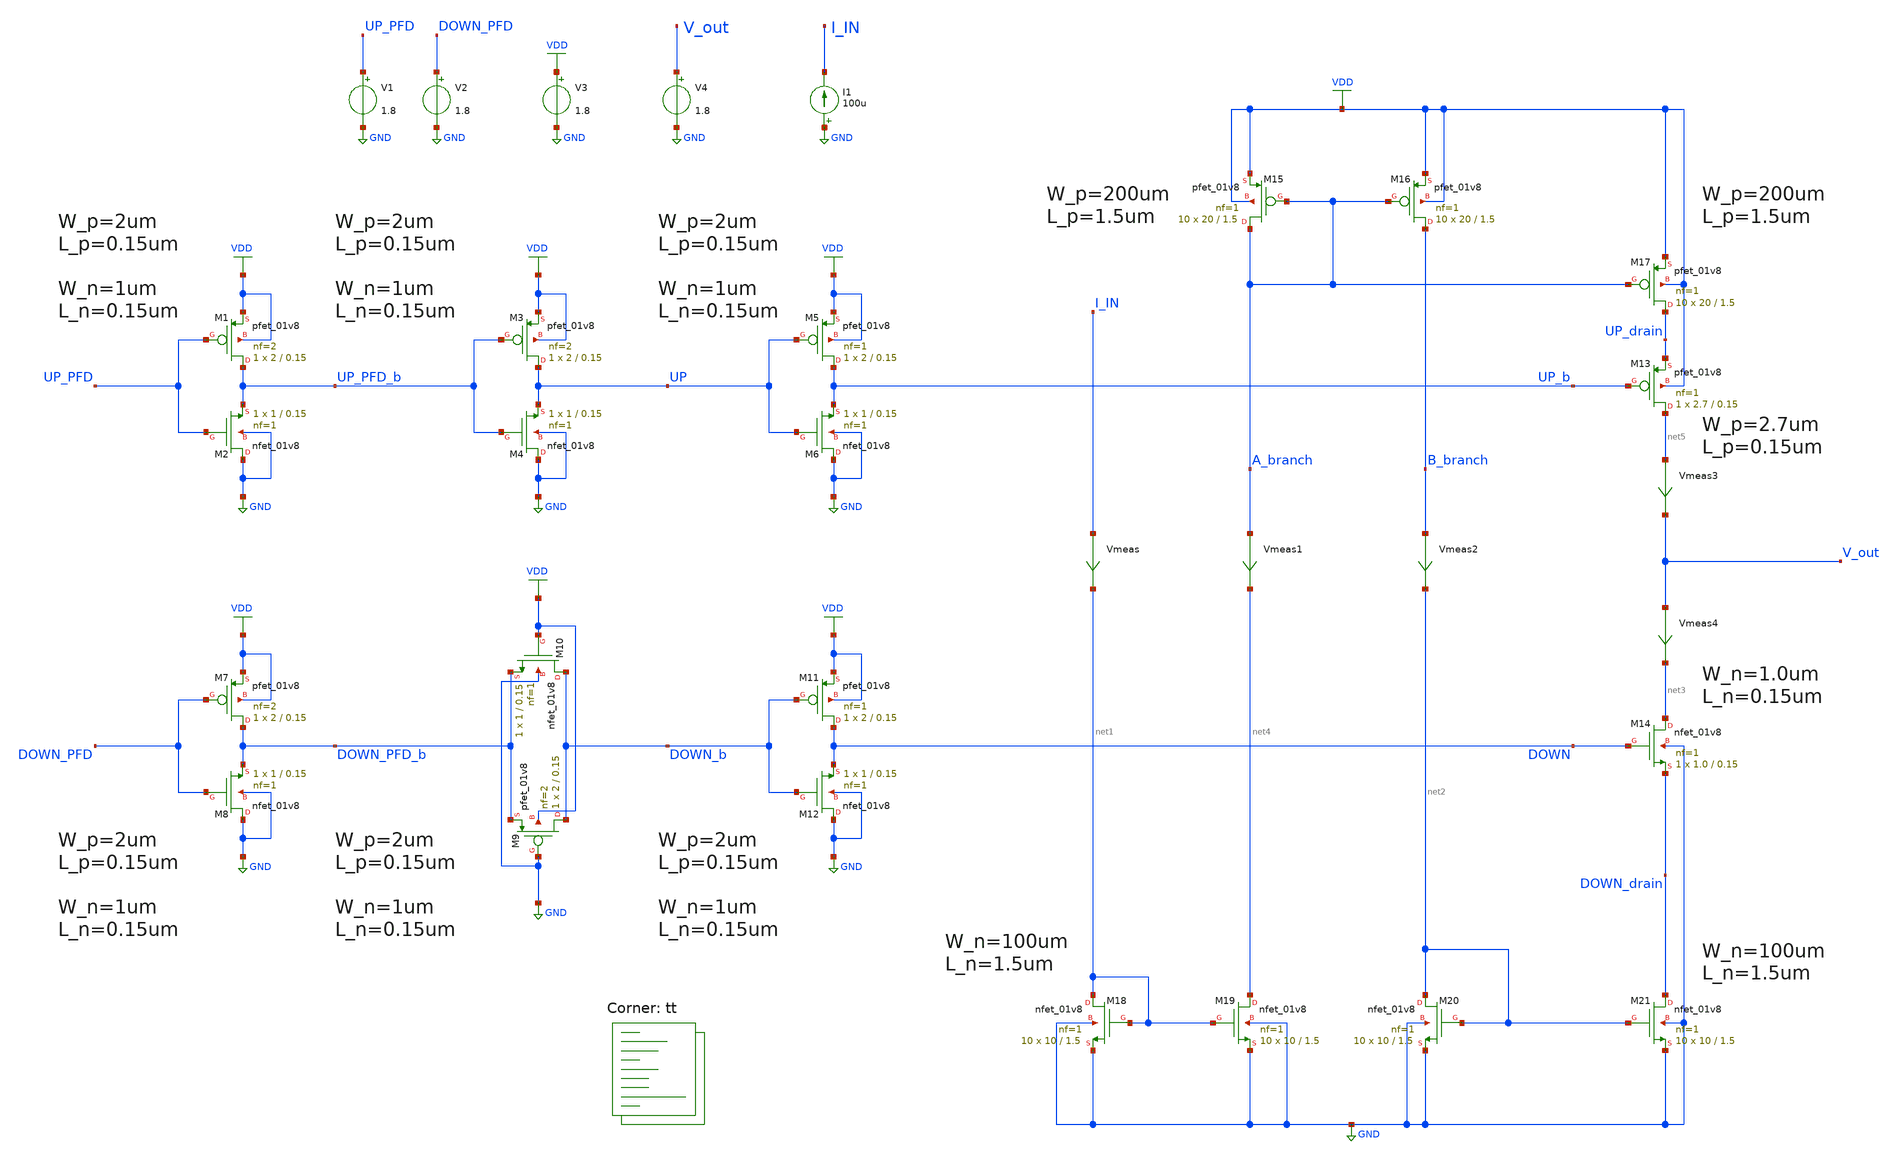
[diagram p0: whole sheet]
** sch_path: projects/pll/charge_pump/xschem_ngspice/charge_pump_DC3.sch
**.subckt charge_pump_DC3
XM18 net1 net1 GND GND sky130_fd_pr__nfet_01v8 L=1.5 W=10 nf=1 ad='int((nf+1)/2) * W/nf * 0.29' as='int((nf+2)/2) * W/nf * 0.29'
+ pd='2*int((nf+1)/2) * (W/nf + 0.29)' ps='2*int((nf+2)/2) * (W/nf + 0.29)' nrd='0.29 / W' nrs='0.29 / W'
+ sa=0 sb=0 sd=0 mult=10 m=10
XM19 net4 net1 GND GND sky130_fd_pr__nfet_01v8 L=1.5 W=10 nf=1 ad='int((nf+1)/2) * W/nf * 0.29' as='int((nf+2)/2) * W/nf * 0.29'
+ pd='2*int((nf+1)/2) * (W/nf + 0.29)' ps='2*int((nf+2)/2) * (W/nf + 0.29)' nrd='0.29 / W' nrs='0.29 / W'
+ sa=0 sb=0 sd=0 mult=10 m=10
Vmeas I_IN net1 0
.save i(vmeas)
XM13 net5 UP_b UP_drain VDD sky130_fd_pr__pfet_01v8 L=0.15 W=2.7 nf=1 ad='int((nf+1)/2) * W/nf * 0.29'
+ as='int((nf+2)/2) * W/nf * 0.29' pd='2*int((nf+1)/2) * (W/nf + 0.29)' ps='2*int((nf+2)/2) * (W/nf + 0.29)'
+ nrd='0.29 / W' nrs='0.29 / W' sa=0 sb=0 sd=0 mult=1 m=1
Vmeas3 net5 V_out 0
.save i(vmeas3)
Vmeas4 V_out net3 0
.save i(vmeas4)
XM14 net3 DOWN DOWN_drain GND sky130_fd_pr__nfet_01v8 L=0.15 W=1.0 nf=1 ad='int((nf+1)/2) * W/nf * 0.29'
+ as='int((nf+2)/2) * W/nf * 0.29' pd='2*int((nf+1)/2) * (W/nf + 0.29)' ps='2*int((nf+2)/2) * (W/nf + 0.29)'
+ nrd='0.29 / W' nrs='0.29 / W' sa=0 sb=0 sd=0 mult=1 m=1
XM17 UP_drain A_branch VDD VDD sky130_fd_pr__pfet_01v8 L=1.5 W=20 nf=1 ad='int((nf+1)/2) * W/nf * 0.29'
+ as='int((nf+2)/2) * W/nf * 0.29' pd='2*int((nf+1)/2) * (W/nf + 0.29)' ps='2*int((nf+2)/2) * (W/nf + 0.29)'
+ nrd='0.29 / W' nrs='0.29 / W' sa=0 sb=0 sd=0 mult=10 m=10
XM21 DOWN_drain net2 GND GND sky130_fd_pr__nfet_01v8 L=1.5 W=10 nf=1 ad='int((nf+1)/2) * W/nf * 0.29'
+ as='int((nf+2)/2) * W/nf * 0.29' pd='2*int((nf+1)/2) * (W/nf + 0.29)' ps='2*int((nf+2)/2) * (W/nf + 0.29)'
+ nrd='0.29 / W' nrs='0.29 / W' sa=0 sb=0 sd=0 mult=10 m=10
XM20 net2 net2 GND GND sky130_fd_pr__nfet_01v8 L=1.5 W=10 nf=1 ad='int((nf+1)/2) * W/nf * 0.29' as='int((nf+2)/2) * W/nf * 0.29'
+ pd='2*int((nf+1)/2) * (W/nf + 0.29)' ps='2*int((nf+2)/2) * (W/nf + 0.29)' nrd='0.29 / W' nrs='0.29 / W'
+ sa=0 sb=0 sd=0 mult=10 m=10
XM15 A_branch A_branch VDD VDD sky130_fd_pr__pfet_01v8 L=1.5 W=20 nf=1 ad='int((nf+1)/2) * W/nf * 0.29'
+ as='int((nf+2)/2) * W/nf * 0.29' pd='2*int((nf+1)/2) * (W/nf + 0.29)' ps='2*int((nf+2)/2) * (W/nf + 0.29)'
+ nrd='0.29 / W' nrs='0.29 / W' sa=0 sb=0 sd=0 mult=10 m=10
XM16 B_branch A_branch VDD VDD sky130_fd_pr__pfet_01v8 L=1.5 W=20 nf=1 ad='int((nf+1)/2) * W/nf * 0.29'
+ as='int((nf+2)/2) * W/nf * 0.29' pd='2*int((nf+1)/2) * (W/nf + 0.29)' ps='2*int((nf+2)/2) * (W/nf + 0.29)'
+ nrd='0.29 / W' nrs='0.29 / W' sa=0 sb=0 sd=0 mult=10 m=10
Vmeas1 A_branch net4 0
.save i(vmeas1)
Vmeas2 B_branch net2 0
.save i(vmeas2)
XM9 DOWN_b GND DOWN_PFD_b VDD sky130_fd_pr__pfet_01v8 L=0.15 W=2 nf=2 ad='int((nf+1)/2) * W/nf * 0.29'
+ as='int((nf+2)/2) * W/nf * 0.29' pd='2*int((nf+1)/2) * (W/nf + 0.29)' ps='2*int((nf+2)/2) * (W/nf + 0.29)'
+ nrd='0.29 / W' nrs='0.29 / W' sa=0 sb=0 sd=0 mult=1 m=1
XM10 DOWN_b VDD DOWN_PFD_b GND sky130_fd_pr__nfet_01v8 L=0.15 W=1 nf=1 ad='int((nf+1)/2) * W/nf * 0.29'
+ as='int((nf+2)/2) * W/nf * 0.29' pd='2*int((nf+1)/2) * (W/nf + 0.29)' ps='2*int((nf+2)/2) * (W/nf + 0.29)'
+ nrd='0.29 / W' nrs='0.29 / W' sa=0 sb=0 sd=0 mult=1 m=1
XM1 UP_PFD_b UP_PFD VDD VDD sky130_fd_pr__pfet_01v8 L=0.15 W=2 nf=2 ad='int((nf+1)/2) * W/nf * 0.29'
+ as='int((nf+2)/2) * W/nf * 0.29' pd='2*int((nf+1)/2) * (W/nf + 0.29)' ps='2*int((nf+2)/2) * (W/nf + 0.29)'
+ nrd='0.29 / W' nrs='0.29 / W' sa=0 sb=0 sd=0 mult=1 m=1
XM2 GND UP_PFD UP_PFD_b GND sky130_fd_pr__nfet_01v8 L=0.15 W=1 nf=1 ad='int((nf+1)/2) * W/nf * 0.29'
+ as='int((nf+2)/2) * W/nf * 0.29' pd='2*int((nf+1)/2) * (W/nf + 0.29)' ps='2*int((nf+2)/2) * (W/nf + 0.29)'
+ nrd='0.29 / W' nrs='0.29 / W' sa=0 sb=0 sd=0 mult=1 m=1
XM7 DOWN_PFD_b DOWN_PFD VDD VDD sky130_fd_pr__pfet_01v8 L=0.15 W=2 nf=2 ad='int((nf+1)/2) * W/nf * 0.29'
+ as='int((nf+2)/2) * W/nf * 0.29' pd='2*int((nf+1)/2) * (W/nf + 0.29)' ps='2*int((nf+2)/2) * (W/nf + 0.29)'
+ nrd='0.29 / W' nrs='0.29 / W' sa=0 sb=0 sd=0 mult=1 m=1
XM8 GND DOWN_PFD DOWN_PFD_b GND sky130_fd_pr__nfet_01v8 L=0.15 W=1 nf=1 ad='int((nf+1)/2) * W/nf * 0.29'
+ as='int((nf+2)/2) * W/nf * 0.29' pd='2*int((nf+1)/2) * (W/nf + 0.29)' ps='2*int((nf+2)/2) * (W/nf + 0.29)'
+ nrd='0.29 / W' nrs='0.29 / W' sa=0 sb=0 sd=0 mult=1 m=1
XM3 UP UP_PFD_b VDD VDD sky130_fd_pr__pfet_01v8 L=0.15 W=2 nf=2 ad='int((nf+1)/2) * W/nf * 0.29' as='int((nf+2)/2) * W/nf * 0.29'
+ pd='2*int((nf+1)/2) * (W/nf + 0.29)' ps='2*int((nf+2)/2) * (W/nf + 0.29)' nrd='0.29 / W' nrs='0.29 / W'
+ sa=0 sb=0 sd=0 mult=1 m=1
XM4 GND UP_PFD_b UP GND sky130_fd_pr__nfet_01v8 L=0.15 W=1 nf=1 ad='int((nf+1)/2) * W/nf * 0.29' as='int((nf+2)/2) * W/nf * 0.29'
+ pd='2*int((nf+1)/2) * (W/nf + 0.29)' ps='2*int((nf+2)/2) * (W/nf + 0.29)' nrd='0.29 / W' nrs='0.29 / W'
+ sa=0 sb=0 sd=0 mult=1 m=1
V3 VDD GND 1.8
I1 GND I_IN 100u
V1 UP_PFD GND 1.8
V2 DOWN_PFD GND 1.8
V4 V_out GND 1.8
XM5 UP_b UP VDD VDD sky130_fd_pr__pfet_01v8 L=0.15 W=2 nf=1 ad='int((nf+1)/2) * W/nf * 0.29' as='int((nf+2)/2) * W/nf * 0.29'
+ pd='2*int((nf+1)/2) * (W/nf + 0.29)' ps='2*int((nf+2)/2) * (W/nf + 0.29)' nrd='0.29 / W' nrs='0.29 / W'
+ sa=0 sb=0 sd=0 mult=1 m=1
XM6 GND UP UP_b GND sky130_fd_pr__nfet_01v8 L=0.15 W=1 nf=1 ad='int((nf+1)/2) * W/nf * 0.29' as='int((nf+2)/2) * W/nf * 0.29'
+ pd='2*int((nf+1)/2) * (W/nf + 0.29)' ps='2*int((nf+2)/2) * (W/nf + 0.29)' nrd='0.29 / W' nrs='0.29 / W'
+ sa=0 sb=0 sd=0 mult=1 m=1
XM11 DOWN DOWN_b VDD VDD sky130_fd_pr__pfet_01v8 L=0.15 W=2 nf=1 ad='int((nf+1)/2) * W/nf * 0.29' as='int((nf+2)/2) * W/nf * 0.29'
+ pd='2*int((nf+1)/2) * (W/nf + 0.29)' ps='2*int((nf+2)/2) * (W/nf + 0.29)' nrd='0.29 / W' nrs='0.29 / W'
+ sa=0 sb=0 sd=0 mult=1 m=1
XM12 GND DOWN_b DOWN GND sky130_fd_pr__nfet_01v8 L=0.15 W=1 nf=1 ad='int((nf+1)/2) * W/nf * 0.29' as='int((nf+2)/2) * W/nf * 0.29'
+ pd='2*int((nf+1)/2) * (W/nf + 0.29)' ps='2*int((nf+2)/2) * (W/nf + 0.29)' nrd='0.29 / W' nrs='0.29 / W'
+ sa=0 sb=0 sd=0 mult=1 m=1
**** begin user architecture code
.lib $::SKYWATER_MODELS/sky130.lib.spice tt



.option method=gear
.option wnflag=1
.option savecurrents

.control
  save all
  dc v4 0 1.8 0.01 v1 0 1.8 1.8
  remzerovec
  write charge_pump_DC3.raw
  set appendwrite
.endc



**** end user architecture code
**.ends
.GLOBAL GND
.GLOBAL VDD
.end
